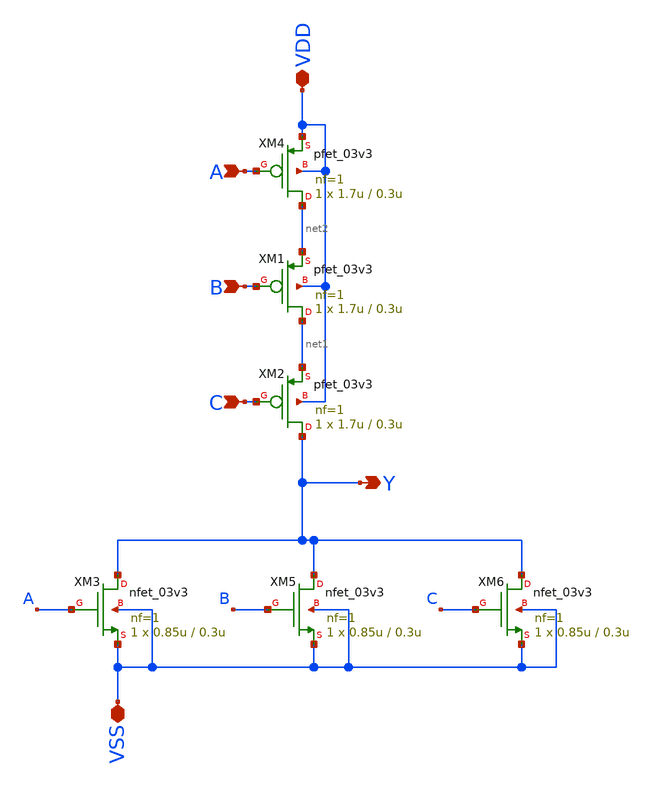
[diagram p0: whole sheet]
** sch_path: gf180mcu_osu_sc_gp12t3v3/xschem/gf180mcu_osu_sc_gp12t3v3__nor3_1.sch
**.subckt gf180mcu_osu_sc_gp12t3v3__nor3_1 A B C VDD Y VSS
*.ipin A
*.ipin B
*.ipin C
*.iopin VDD
*.opin Y
*.iopin VSS
XM4 net2 A VDD VDD pfet_03v3 L=0.3u W=1.7u nf=1 ad='int((nf+1)/2) * W/nf * 0.18u' as='int((nf+2)/2) * W/nf * 0.18u'
+ pd='2*int((nf+1)/2) * (W/nf + 0.18u)' ps='2*int((nf+2)/2) * (W/nf + 0.18u)' nrd='0.18u / W' nrs='0.18u / W'
+ sa=0 sb=0 sd=0 m=1
XM3 Y A VSS VSS nfet_03v3 L=0.3u W=0.85u nf=1 ad='int((nf+1)/2) * W/nf * 0.18u' as='int((nf+2)/2) * W/nf * 0.18u'
+ pd='2*int((nf+1)/2) * (W/nf + 0.18u)' ps='2*int((nf+2)/2) * (W/nf + 0.18u)' nrd='0.18u / W' nrs='0.18u / W'
+ sa=0 sb=0 sd=0 m=1
XM1 net1 B net2 VDD pfet_03v3 L=0.3u W=1.7u nf=1 ad='int((nf+1)/2) * W/nf * 0.18u' as='int((nf+2)/2) * W/nf * 0.18u'
+ pd='2*int((nf+1)/2) * (W/nf + 0.18u)' ps='2*int((nf+2)/2) * (W/nf + 0.18u)' nrd='0.18u / W' nrs='0.18u / W'
+ sa=0 sb=0 sd=0 m=1
XM2 Y C net1 VDD pfet_03v3 L=0.3u W=1.7u nf=1 ad='int((nf+1)/2) * W/nf * 0.18u' as='int((nf+2)/2) * W/nf * 0.18u'
+ pd='2*int((nf+1)/2) * (W/nf + 0.18u)' ps='2*int((nf+2)/2) * (W/nf + 0.18u)' nrd='0.18u / W' nrs='0.18u / W'
+ sa=0 sb=0 sd=0 m=1
XM5 Y B VSS VSS nfet_03v3 L=0.3u W=0.85u nf=1 ad='int((nf+1)/2) * W/nf * 0.18u' as='int((nf+2)/2) * W/nf * 0.18u'
+ pd='2*int((nf+1)/2) * (W/nf + 0.18u)' ps='2*int((nf+2)/2) * (W/nf + 0.18u)' nrd='0.18u / W' nrs='0.18u / W'
+ sa=0 sb=0 sd=0 m=1
XM6 Y C VSS VSS nfet_03v3 L=0.3u W=0.85u nf=1 ad='int((nf+1)/2) * W/nf * 0.18u' as='int((nf+2)/2) * W/nf * 0.18u'
+ pd='2*int((nf+1)/2) * (W/nf + 0.18u)' ps='2*int((nf+2)/2) * (W/nf + 0.18u)' nrd='0.18u / W' nrs='0.18u / W'
+ sa=0 sb=0 sd=0 m=1
**.ends
.end
